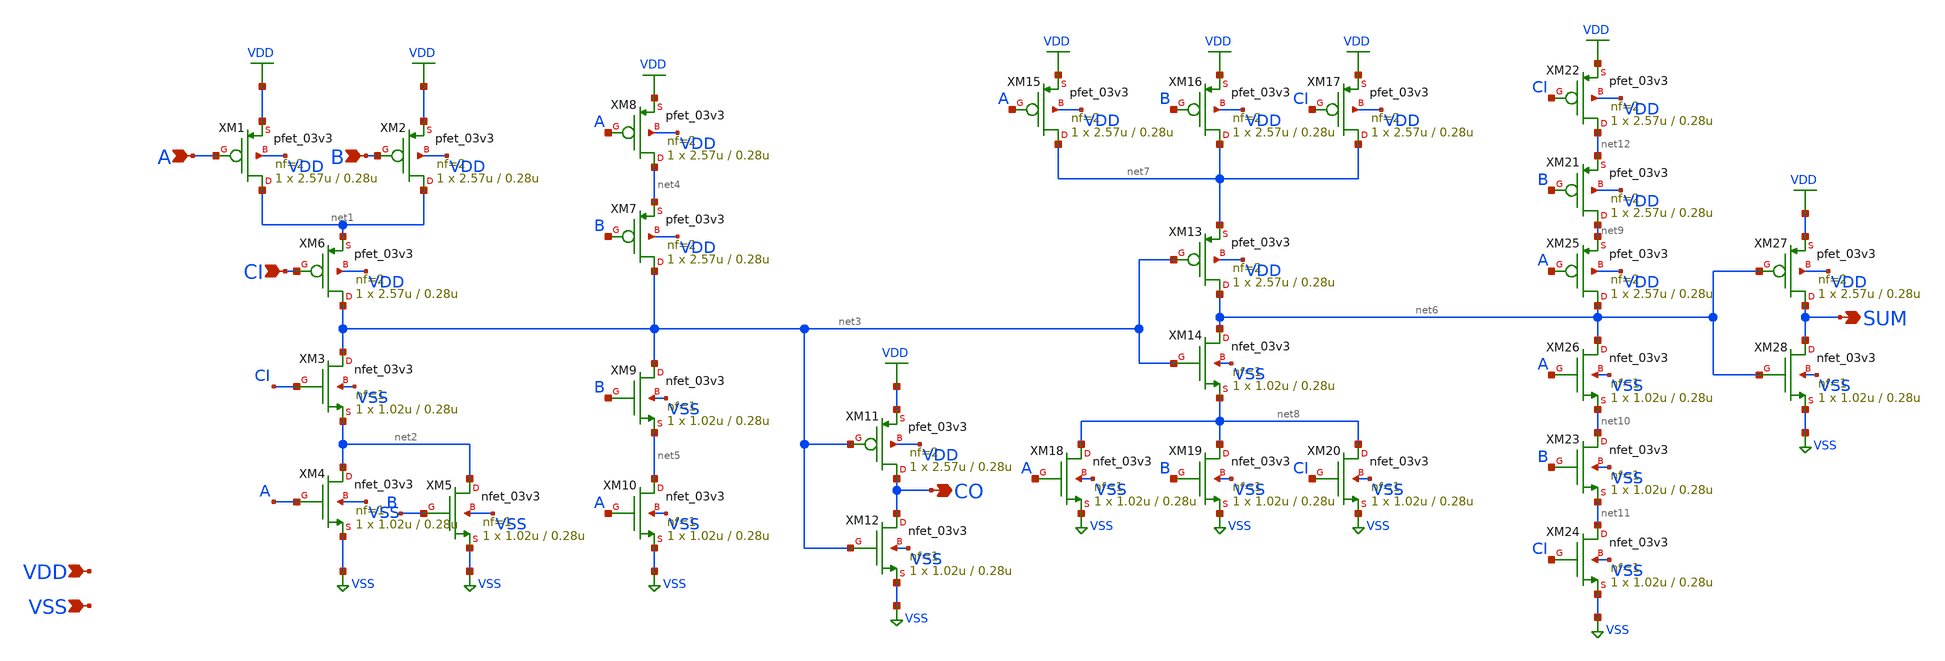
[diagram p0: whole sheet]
** sch_path: xschem/gf180mcu_ocd_sc_rt12t3v3__addf_1.sch
**.subckt gf180mcu_ocd_sc_rt12t3v3__addf_1 A B CI SUM CO VDD VSS
*.ipin A
*.ipin B
*.ipin CI
*.opin SUM
*.opin CO
*.ipin VDD
*.ipin VSS
XM1 net1 A VDD VDD pfet_03v3 L=0.28u W=2.57u nf=2 ad='int((nf+1)/2) * W/nf * 0.18u' as='int((nf+2)/2) * W/nf * 0.18u'
+ pd='2*int((nf+1)/2) * (W/nf + 0.18u)' ps='2*int((nf+2)/2) * (W/nf + 0.18u)' nrd='0.18u / W' nrs='0.18u / W'
+ sa=0 sb=0 sd=0 m=1
XM2 net1 B VDD VDD pfet_03v3 L=0.28u W=2.57u nf=2 ad='int((nf+1)/2) * W/nf * 0.18u' as='int((nf+2)/2) * W/nf * 0.18u'
+ pd='2*int((nf+1)/2) * (W/nf + 0.18u)' ps='2*int((nf+2)/2) * (W/nf + 0.18u)' nrd='0.18u / W' nrs='0.18u / W'
+ sa=0 sb=0 sd=0 m=1
XM3 net3 CI net2 VSS nfet_03v3 L=0.28u W=1.02u nf=1 ad='int((nf+1)/2) * W/nf * 0.18u' as='int((nf+2)/2) * W/nf * 0.18u'
+ pd='2*int((nf+1)/2) * (W/nf + 0.18u)' ps='2*int((nf+2)/2) * (W/nf + 0.18u)' nrd='0.18u / W' nrs='0.18u / W'
+ sa=0 sb=0 sd=0 m=1
XM4 net2 A VSS VSS nfet_03v3 L=0.28u W=1.02u nf=1 ad='int((nf+1)/2) * W/nf * 0.18u' as='int((nf+2)/2) * W/nf * 0.18u'
+ pd='2*int((nf+1)/2) * (W/nf + 0.18u)' ps='2*int((nf+2)/2) * (W/nf + 0.18u)' nrd='0.18u / W' nrs='0.18u / W'
+ sa=0 sb=0 sd=0 m=1
XM5 net2 B VSS VSS nfet_03v3 L=0.28u W=1.02u nf=1 ad='int((nf+1)/2) * W/nf * 0.18u' as='int((nf+2)/2) * W/nf * 0.18u'
+ pd='2*int((nf+1)/2) * (W/nf + 0.18u)' ps='2*int((nf+2)/2) * (W/nf + 0.18u)' nrd='0.18u / W' nrs='0.18u / W'
+ sa=0 sb=0 sd=0 m=1
XM6 net3 CI net1 VDD pfet_03v3 L=0.28u W=2.57u nf=2 ad='int((nf+1)/2) * W/nf * 0.18u' as='int((nf+2)/2) * W/nf * 0.18u'
+ pd='2*int((nf+1)/2) * (W/nf + 0.18u)' ps='2*int((nf+2)/2) * (W/nf + 0.18u)' nrd='0.18u / W' nrs='0.18u / W'
+ sa=0 sb=0 sd=0 m=1
XM7 net3 B net4 VDD pfet_03v3 L=0.28u W=2.57u nf=2 ad='int((nf+1)/2) * W/nf * 0.18u' as='int((nf+2)/2) * W/nf * 0.18u'
+ pd='2*int((nf+1)/2) * (W/nf + 0.18u)' ps='2*int((nf+2)/2) * (W/nf + 0.18u)' nrd='0.18u / W' nrs='0.18u / W'
+ sa=0 sb=0 sd=0 m=1
XM8 net4 A VDD VDD pfet_03v3 L=0.28u W=2.57u nf=2 ad='int((nf+1)/2) * W/nf * 0.18u' as='int((nf+2)/2) * W/nf * 0.18u'
+ pd='2*int((nf+1)/2) * (W/nf + 0.18u)' ps='2*int((nf+2)/2) * (W/nf + 0.18u)' nrd='0.18u / W' nrs='0.18u / W'
+ sa=0 sb=0 sd=0 m=1
XM9 net3 B net5 VSS nfet_03v3 L=0.28u W=1.02u nf=1 ad='int((nf+1)/2) * W/nf * 0.18u' as='int((nf+2)/2) * W/nf * 0.18u'
+ pd='2*int((nf+1)/2) * (W/nf + 0.18u)' ps='2*int((nf+2)/2) * (W/nf + 0.18u)' nrd='0.18u / W' nrs='0.18u / W'
+ sa=0 sb=0 sd=0 m=1
XM10 net5 A VSS VSS nfet_03v3 L=0.28u W=1.02u nf=1 ad='int((nf+1)/2) * W/nf * 0.18u' as='int((nf+2)/2) * W/nf * 0.18u'
+ pd='2*int((nf+1)/2) * (W/nf + 0.18u)' ps='2*int((nf+2)/2) * (W/nf + 0.18u)' nrd='0.18u / W' nrs='0.18u / W'
+ sa=0 sb=0 sd=0 m=1
XM11 CO net3 VDD VDD pfet_03v3 L=0.28u W=2.57u nf=2 ad='int((nf+1)/2) * W/nf * 0.18u' as='int((nf+2)/2) * W/nf * 0.18u'
+ pd='2*int((nf+1)/2) * (W/nf + 0.18u)' ps='2*int((nf+2)/2) * (W/nf + 0.18u)' nrd='0.18u / W' nrs='0.18u / W'
+ sa=0 sb=0 sd=0 m=1
XM12 CO net3 VSS VSS nfet_03v3 L=0.28u W=1.02u nf=1 ad='int((nf+1)/2) * W/nf * 0.18u' as='int((nf+2)/2) * W/nf * 0.18u'
+ pd='2*int((nf+1)/2) * (W/nf + 0.18u)' ps='2*int((nf+2)/2) * (W/nf + 0.18u)' nrd='0.18u / W' nrs='0.18u / W'
+ sa=0 sb=0 sd=0 m=1
XM13 net6 net3 net7 VDD pfet_03v3 L=0.28u W=2.57u nf=2 ad='int((nf+1)/2) * W/nf * 0.18u' as='int((nf+2)/2) * W/nf * 0.18u'
+ pd='2*int((nf+1)/2) * (W/nf + 0.18u)' ps='2*int((nf+2)/2) * (W/nf + 0.18u)' nrd='0.18u / W' nrs='0.18u / W'
+ sa=0 sb=0 sd=0 m=1
XM14 net6 net3 net8 VSS nfet_03v3 L=0.28u W=1.02u nf=1 ad='int((nf+1)/2) * W/nf * 0.18u' as='int((nf+2)/2) * W/nf * 0.18u'
+ pd='2*int((nf+1)/2) * (W/nf + 0.18u)' ps='2*int((nf+2)/2) * (W/nf + 0.18u)' nrd='0.18u / W' nrs='0.18u / W'
+ sa=0 sb=0 sd=0 m=1
XM15 net7 A VDD VDD pfet_03v3 L=0.28u W=2.57u nf=2 ad='int((nf+1)/2) * W/nf * 0.18u' as='int((nf+2)/2) * W/nf * 0.18u'
+ pd='2*int((nf+1)/2) * (W/nf + 0.18u)' ps='2*int((nf+2)/2) * (W/nf + 0.18u)' nrd='0.18u / W' nrs='0.18u / W'
+ sa=0 sb=0 sd=0 m=1
XM16 net7 B VDD VDD pfet_03v3 L=0.28u W=2.57u nf=2 ad='int((nf+1)/2) * W/nf * 0.18u' as='int((nf+2)/2) * W/nf * 0.18u'
+ pd='2*int((nf+1)/2) * (W/nf + 0.18u)' ps='2*int((nf+2)/2) * (W/nf + 0.18u)' nrd='0.18u / W' nrs='0.18u / W'
+ sa=0 sb=0 sd=0 m=1
XM17 net7 CI VDD VDD pfet_03v3 L=0.28u W=2.57u nf=2 ad='int((nf+1)/2) * W/nf * 0.18u' as='int((nf+2)/2) * W/nf * 0.18u'
+ pd='2*int((nf+1)/2) * (W/nf + 0.18u)' ps='2*int((nf+2)/2) * (W/nf + 0.18u)' nrd='0.18u / W' nrs='0.18u / W'
+ sa=0 sb=0 sd=0 m=1
XM18 net8 A VSS VSS nfet_03v3 L=0.28u W=1.02u nf=1 ad='int((nf+1)/2) * W/nf * 0.18u' as='int((nf+2)/2) * W/nf * 0.18u'
+ pd='2*int((nf+1)/2) * (W/nf + 0.18u)' ps='2*int((nf+2)/2) * (W/nf + 0.18u)' nrd='0.18u / W' nrs='0.18u / W'
+ sa=0 sb=0 sd=0 m=1
XM19 net8 B VSS VSS nfet_03v3 L=0.28u W=1.02u nf=1 ad='int((nf+1)/2) * W/nf * 0.18u' as='int((nf+2)/2) * W/nf * 0.18u'
+ pd='2*int((nf+1)/2) * (W/nf + 0.18u)' ps='2*int((nf+2)/2) * (W/nf + 0.18u)' nrd='0.18u / W' nrs='0.18u / W'
+ sa=0 sb=0 sd=0 m=1
XM20 net8 CI VSS VSS nfet_03v3 L=0.28u W=1.02u nf=1 ad='int((nf+1)/2) * W/nf * 0.18u' as='int((nf+2)/2) * W/nf * 0.18u'
+ pd='2*int((nf+1)/2) * (W/nf + 0.18u)' ps='2*int((nf+2)/2) * (W/nf + 0.18u)' nrd='0.18u / W' nrs='0.18u / W'
+ sa=0 sb=0 sd=0 m=1
XM21 net9 B net12 VDD pfet_03v3 L=0.28u W=2.57u nf=2 ad='int((nf+1)/2) * W/nf * 0.18u' as='int((nf+2)/2) * W/nf * 0.18u'
+ pd='2*int((nf+1)/2) * (W/nf + 0.18u)' ps='2*int((nf+2)/2) * (W/nf + 0.18u)' nrd='0.18u / W' nrs='0.18u / W'
+ sa=0 sb=0 sd=0 m=1
XM22 net12 CI VDD VDD pfet_03v3 L=0.28u W=2.57u nf=2 ad='int((nf+1)/2) * W/nf * 0.18u' as='int((nf+2)/2) * W/nf * 0.18u'
+ pd='2*int((nf+1)/2) * (W/nf + 0.18u)' ps='2*int((nf+2)/2) * (W/nf + 0.18u)' nrd='0.18u / W' nrs='0.18u / W'
+ sa=0 sb=0 sd=0 m=1
XM23 net10 B net11 VSS nfet_03v3 L=0.28u W=1.02u nf=1 ad='int((nf+1)/2) * W/nf * 0.18u' as='int((nf+2)/2) * W/nf * 0.18u'
+ pd='2*int((nf+1)/2) * (W/nf + 0.18u)' ps='2*int((nf+2)/2) * (W/nf + 0.18u)' nrd='0.18u / W' nrs='0.18u / W'
+ sa=0 sb=0 sd=0 m=1
XM24 net11 CI VSS VSS nfet_03v3 L=0.28u W=1.02u nf=1 ad='int((nf+1)/2) * W/nf * 0.18u' as='int((nf+2)/2) * W/nf * 0.18u'
+ pd='2*int((nf+1)/2) * (W/nf + 0.18u)' ps='2*int((nf+2)/2) * (W/nf + 0.18u)' nrd='0.18u / W' nrs='0.18u / W'
+ sa=0 sb=0 sd=0 m=1
XM25 net6 A net9 VDD pfet_03v3 L=0.28u W=2.57u nf=2 ad='int((nf+1)/2) * W/nf * 0.18u' as='int((nf+2)/2) * W/nf * 0.18u'
+ pd='2*int((nf+1)/2) * (W/nf + 0.18u)' ps='2*int((nf+2)/2) * (W/nf + 0.18u)' nrd='0.18u / W' nrs='0.18u / W'
+ sa=0 sb=0 sd=0 m=1
XM26 net6 A net10 VSS nfet_03v3 L=0.28u W=1.02u nf=1 ad='int((nf+1)/2) * W/nf * 0.18u' as='int((nf+2)/2) * W/nf * 0.18u'
+ pd='2*int((nf+1)/2) * (W/nf + 0.18u)' ps='2*int((nf+2)/2) * (W/nf + 0.18u)' nrd='0.18u / W' nrs='0.18u / W'
+ sa=0 sb=0 sd=0 m=1
XM27 SUM net6 VDD VDD pfet_03v3 L=0.28u W=2.57u nf=2 ad='int((nf+1)/2) * W/nf * 0.18u' as='int((nf+2)/2) * W/nf * 0.18u'
+ pd='2*int((nf+1)/2) * (W/nf + 0.18u)' ps='2*int((nf+2)/2) * (W/nf + 0.18u)' nrd='0.18u / W' nrs='0.18u / W'
+ sa=0 sb=0 sd=0 m=1
XM28 SUM net6 VSS VSS nfet_03v3 L=0.28u W=1.02u nf=1 ad='int((nf+1)/2) * W/nf * 0.18u' as='int((nf+2)/2) * W/nf * 0.18u'
+ pd='2*int((nf+1)/2) * (W/nf + 0.18u)' ps='2*int((nf+2)/2) * (W/nf + 0.18u)' nrd='0.18u / W' nrs='0.18u / W'
+ sa=0 sb=0 sd=0 m=1
**.ends
.GLOBAL VDD
.GLOBAL VSS
.end
